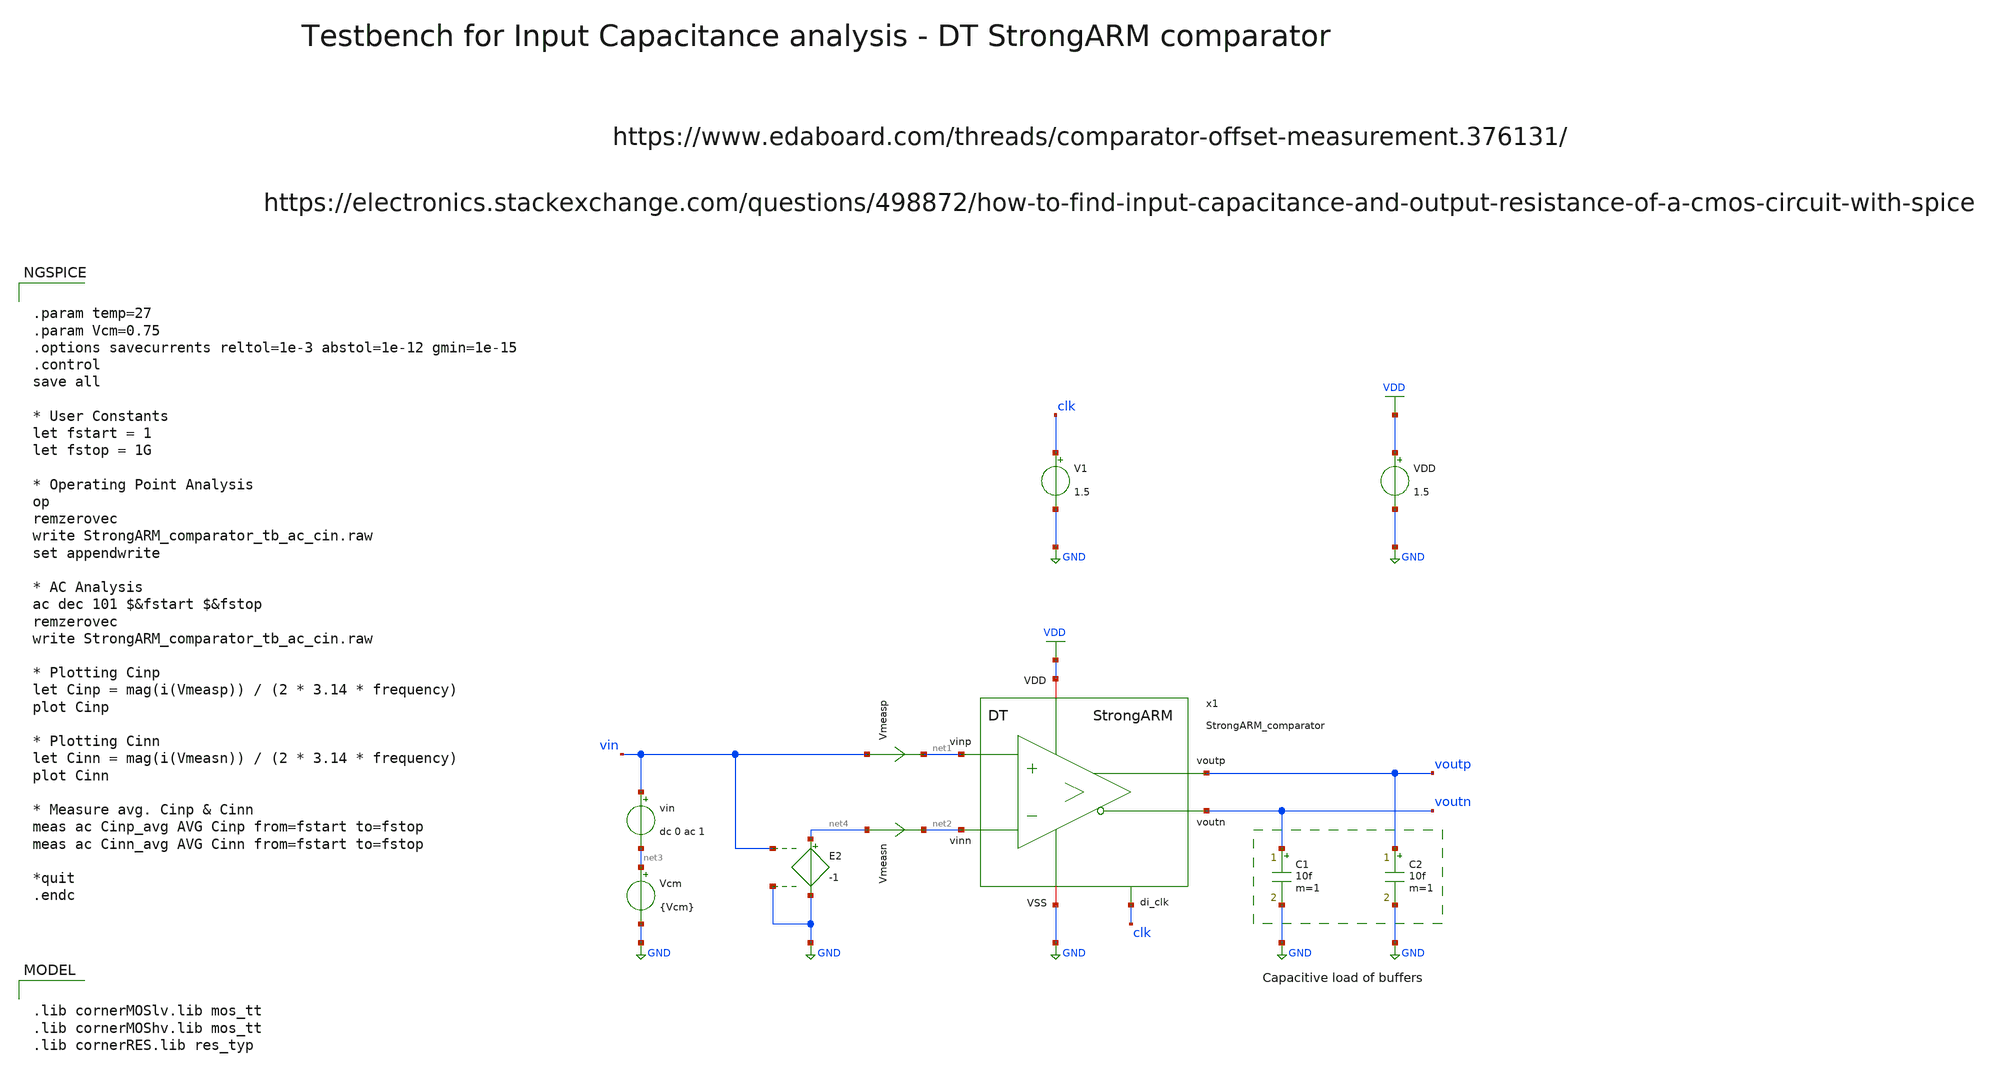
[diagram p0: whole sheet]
** sch_path: SG13G2_ATBS-ADC-main/xschem/comparator/discrete_time/StrongARM/testbenches/StrongARM_comparator_tb_ac_cin.sch
**.subckt StrongARM_comparator_tb_ac_cin
VDD VDD GND 1.5
V1 clk GND 1.5
C1 voutn GND 10f m=1
C2 voutp GND 10f m=1
Vmeasp vin net1 0
.save i(vmeasp)
Vmeasn net4 net2 0
.save i(vmeasn)
vin vin net3 dc 0 ac 1
Vcm net3 GND {Vcm}
E2 net4 GND vin GND -1
x1 clk VDD voutp net1 GND voutn net2 StrongARM_comparator
**** begin user architecture code

.lib cornerMOSlv.lib mos_tt
.lib cornerMOShv.lib mos_tt
.lib cornerRES.lib res_typ



.param temp=27
.param Vcm=0.75
.options savecurrents reltol=1e-3 abstol=1e-12 gmin=1e-15
.control
save all

* User Constants
let fstart = 1
let fstop = 1G

* Operating Point Analysis
op
remzerovec
write StrongARM_comparator_tb_ac_cin.raw
set appendwrite

* AC Analysis
ac dec 101 $&fstart $&fstop
remzerovec
write StrongARM_comparator_tb_ac_cin.raw

* Plotting Cinp
let Cinp = mag(i(Vmeasp)) / (2 * 3.14 * frequency)
plot Cinp

* Plotting Cinn
let Cinn = mag(i(Vmeasn)) / (2 * 3.14 * frequency)
plot Cinn

* Measure avg. Cinp & Cinn
meas ac Cinp_avg AVG Cinp from=fstart to=fstop
meas ac Cinn_avg AVG Cinn from=fstart to=fstop

*quit
.endc

**** end user architecture code
**.ends

* expanding   symbol:  comparator/discrete_time/StrongARM/StrongARM_comparator.sym # of pins=7
** sym_path: SG13G2_ATBS-ADC-main/xschem/comparator/discrete_time/StrongARM/StrongARM_comparator.sym
** sch_path: SG13G2_ATBS-ADC-main/xschem/comparator/discrete_time/StrongARM/StrongARM_comparator.sch
.subckt StrongARM_comparator di_clk VDD voutp vinp VSS voutn vinn
*.iopin VDD
*.opin voutp
*.iopin VSS
*.opin voutn
*.ipin vinp
*.ipin vinn
*.ipin di_clk
XM1 net1 vinp vs VSS sg13_lv_nmos w=1.0u l=0.13u ng=1 m=1 mm_ok=1
XM2 net2 vinn vs VSS sg13_lv_nmos w=1.0u l=0.13u ng=1 m=1 mm_ok=1
XM3 voutn voutp net1 VSS sg13_lv_nmos w=1.0u l=0.13u ng=1 m=1 mm_ok=1
XM4 voutp voutn net2 VSS sg13_lv_nmos w=1.0u l=0.13u ng=1 m=1 mm_ok=1
XM5 voutn voutp VDD VDD sg13_lv_pmos w=1.0u l=0.13u ng=1 m=1 mm_ok=1
XM6 voutp voutn VDD VDD sg13_lv_pmos w=1.0u l=0.13u ng=1 m=1 mm_ok=1
XM7 vs di_clk VSS VSS sg13_lv_nmos w=1.0u l=0.13u ng=1 m=1 mm_ok=1
XM8 voutn di_clk VDD VDD sg13_lv_pmos w=1.0u l=0.13u ng=1 m=1 mm_ok=1
XM9 net1 di_clk VDD VDD sg13_lv_pmos w=1.0u l=0.13u ng=1 m=1 mm_ok=1
XM10 voutp di_clk VDD VDD sg13_lv_pmos w=1.0u l=0.13u ng=1 m=1 mm_ok=1
XM11 net2 di_clk VDD VDD sg13_lv_pmos w=1.0u l=0.13u ng=1 m=1 mm_ok=1
CPn voutn VSS 300f m=1
CPp voutp VSS 300f m=1
.ends

.GLOBAL GND
.GLOBAL VDD
.end
